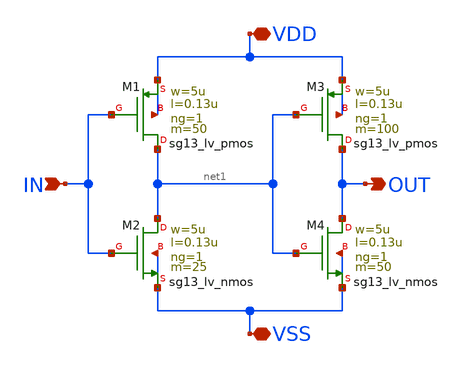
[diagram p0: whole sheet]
** sch_path: SSDOR_1V_v1/components/trans_gate/tg_buff.sch
**.subckt tg_buff VSS VDD IN OUT
*.iopin VSS
*.iopin VDD
*.ipin IN
*.opin OUT
XM1 net1 IN VDD VDD sg13_lv_pmos w=5u l=0.13u ng=1 m=50 mm_ok=1
XM2 net1 IN VSS VSS sg13_lv_nmos w=5u l=0.13u ng=1 m=25 mm_ok=1
XM3 OUT net1 VDD VDD sg13_lv_pmos w=5u l=0.13u ng=1 m=100 mm_ok=1
XM4 OUT net1 VSS VSS sg13_lv_nmos w=5u l=0.13u ng=1 m=50 mm_ok=1
**.ends
.end
